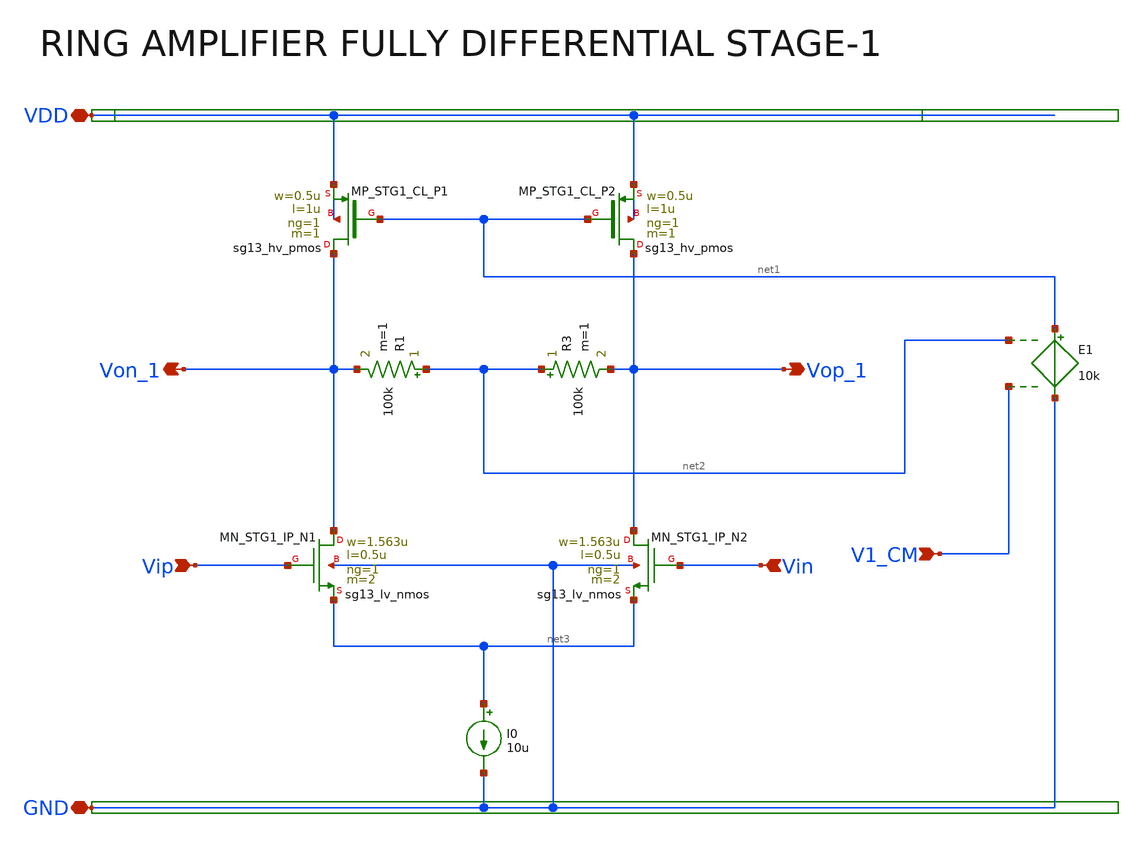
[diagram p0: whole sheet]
** sch_path: Design Files/RAMP/Fully-Diff-RAMP/STG1-FD.sch
**.subckt STG1-FD Von_1 VDD GND Vop_1 Vip Vin V1_CM
*.opin Von_1
*.iopin VDD
*.iopin GND
*.opin Vop_1
*.ipin Vip
*.ipin Vin
*.ipin V1_CM
R1 net2 Von_1 100k m=1
R3 net2 Vop_1 100k m=1
XMN_STG1_IP_N1 Von_1 Vip net3 GND sg13_lv_nmos w=1.563u l=0.5u ng=1 m=2 mm_ok=1
XMN_STG1_IP_N2 Vop_1 Vin net3 GND sg13_lv_nmos w=1.563u l=0.5u ng=1 m=2 mm_ok=1
I0 net3 GND 10u
XMP_STG1_CL_P1 Von_1 net1 VDD VDD sg13_hv_pmos w=0.5u l=1u ng=1 m=1 mm_ok=1
XMP_STG1_CL_P2 Vop_1 net1 VDD VDD sg13_hv_pmos w=0.5u l=1u ng=1 m=1 mm_ok=1
E1 net1 GND net2 V1_CM 10k
**.ends
.end
